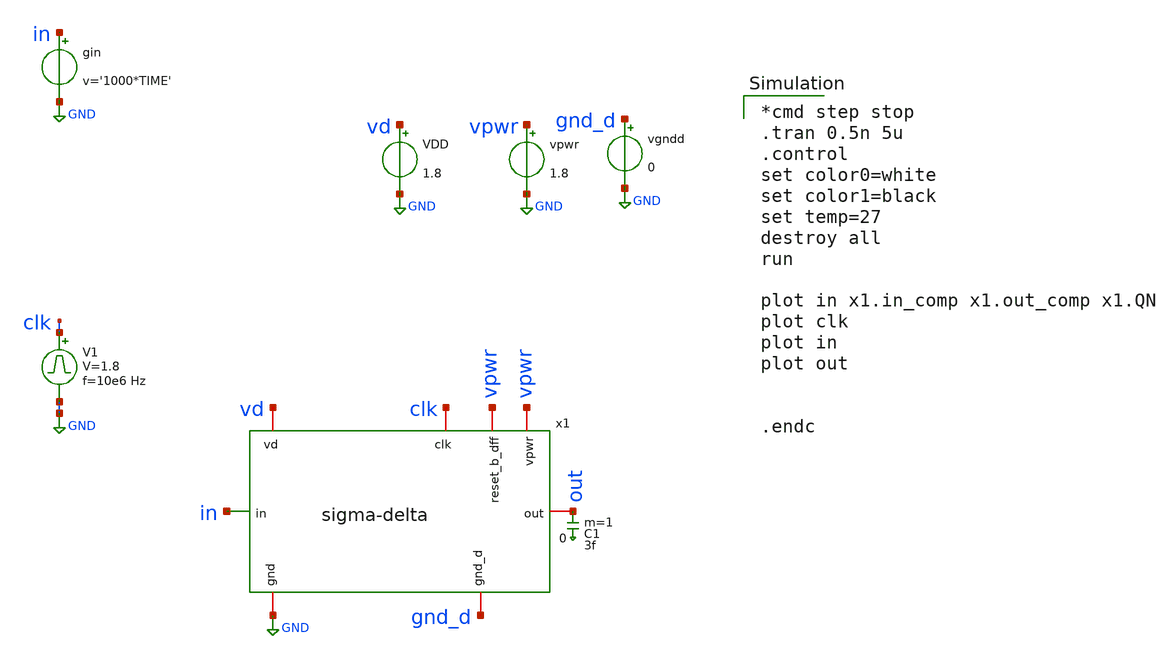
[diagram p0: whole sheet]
** sch_path: sigma-delta_modulator/xschem/sigma_tb-tran.sch
* Copyright 2020 Stefan Frederik Schippers
* Licensed under the Apache License, Version 2.0 (the "License");
* you may not use this file except in compliance with the License.
* You may obtain a copy of the License at
* https://www.apache.org/licenses/LICENSE-2.0
* Unless required by applicable law or agreed to in writing, software
* distributed under the License is distributed on an "AS IS" BASIS,
* WITHOUT WARRANTIES OR CONDITIONS OF ANY KIND, either express or implied.
* See the License for the specific language governing permissions and
* limitations under the License.
**.subckt sigma_tb-tran
VDD vd GND 1.8
gin in GND v='1000*TIME'
V1 clk GND pulse 0 1.8 '0.495/ 10e6 ' '0.01/10e6 ' '0.01/10e6 ' '0.49/10e6 ' '1/10e6 '
x1 gnd_d vpwr clk vd out in vpwr GND sigma-delta
vpwr vpwr GND 1.8
vgndd gnd_d GND 0
C1 out 0 3f m=1
**** begin user architecture code

*cmd step stop
.tran 0.5n 5u
.control
set color0=white
set color1=black
set temp=27
destroy all
run

plot in x1.in_comp x1.out_comp x1.QN
plot clk
plot in
plot out


.endc

 .lib $::SKYWATER_MODELS/sky130.lib.spice tt
.include $::SKYWATER_STDCELLS/sky130_fd_sc_hd.spice

**** end user architecture code
**.ends

* expanding   symbol:
*+  /home/hugodg/projects-sky130/temp-sensor/sigma-delta_modulator/xschem/sigma-delta.sym # of pins=8
** sym_path: sigma-delta_modulator/xschem/sigma-delta.sym
** sch_path: sigma-delta_modulator/xschem/sigma-delta.sch
.subckt sigma-delta gnd_d vpwr clk vd out in reset_b_dff gnd
*.ipin in
*.iopin gnd
*.iopin clk
*.iopin out
*.iopin reset_b_dff
*.iopin vpwr
*.iopin gnd_d
*.iopin vd
**** begin user architecture code




**** end user architecture code
XC1 in_comp gnd sky130_fd_pr__cap_mim_m3_1 W=27.196 L=27.196 MF=1 m=1
XR2 QN in_comp gnd sky130_fd_pr__res_xhigh_po_0p35 L=37 mult=1 m=1
x2 clk out_comp reset_b_dff gnd_d gnd_d vpwr vpwr out QN sky130_fd_sc_hd__dfrbp_1
XR1 in_comp in gnd sky130_fd_pr__res_xhigh_po_0p35 L=37 mult=1 m=1
x1 in_comp gnd_d gnd_d vpwr VPWR out_comp sky130_fd_sc_hd__inv_1
.ends

.GLOBAL GND
.end
